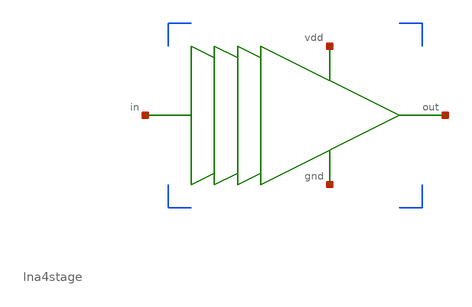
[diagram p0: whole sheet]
** sch_path: xschem/user_analog_project_wrapper.sch
**.subckt user_analog_project_wrapper
XFLNA1 net1 net2 net3 net4 lna4stage
**** begin user architecture code


.lib /foss/pdk/sky130A/libs.tech/ngspice/sky130.lib.spice tt
.control
	** dc V1 0.769 3.769 0.01
	** dc V2 0 3 0.01
        ** SIN(0.9 0.00001 700000000)
	tran 0.0000000001 0.000001
	** ac lin 500 1K 100MEG
	** plot vdb(out1) xlog
.endc
.save all


 ** manual skywater pdks install (with patches applied)
* .lib $::SKYWATER_MODELS/models/sky130.lib.spice tt

** opencircuitdesign pdks install
.lib /foss/pdk/sky130A/libs.tech/ngspice/sky130.lib.spice tt

.param mc_mm_switch=0
.param mc_pr_switch=0

**** end user architecture code
**.ends
.end
